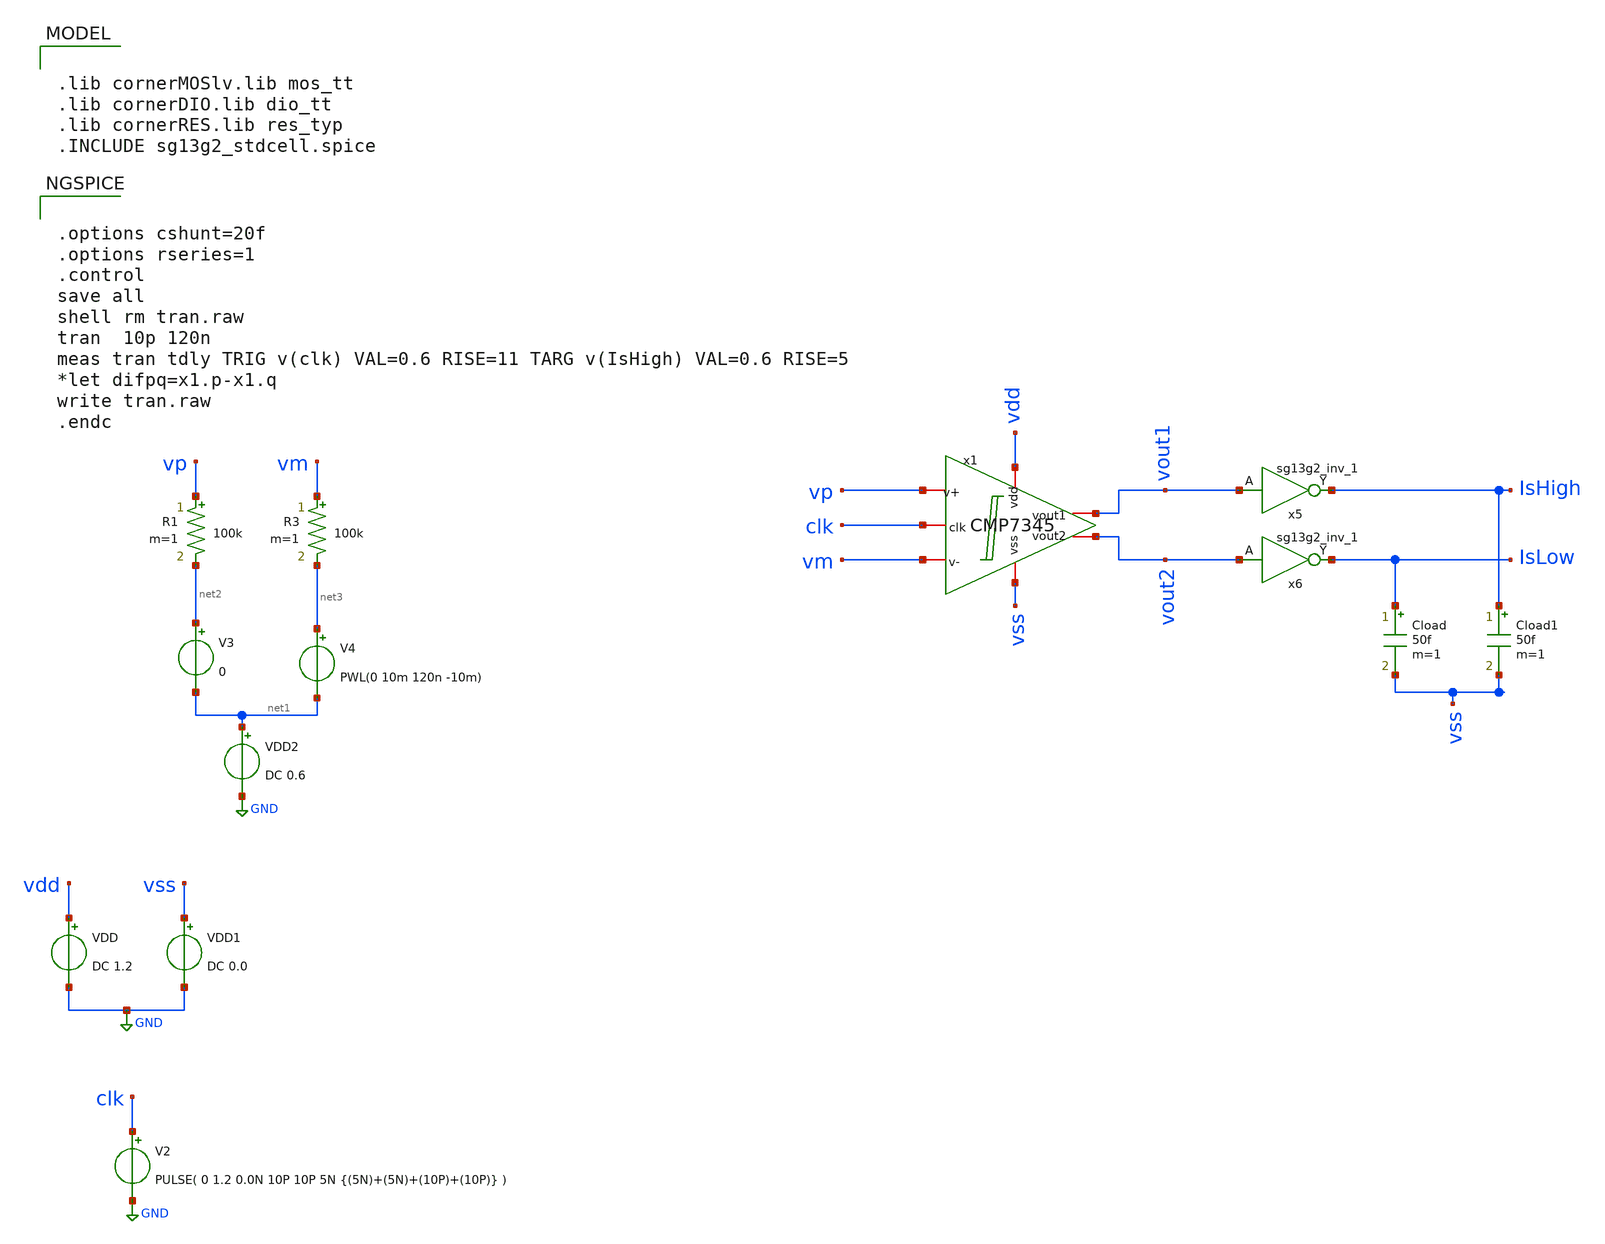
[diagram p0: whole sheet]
** sch_path: CMP7345-main/testbenches/noise/xschem/CMP7345_kickback.sch
**.subckt CMP7345_kickback
VDD vdd GND DC 1.2
Cload IsLow vss 50f m=1
x1 vdd vout1 vout2 vp vm clk vss CMP7345
VDD1 vss GND DC 0.0
Cload1 IsHigh vss 50f m=1
V2 clk GND PULSE( 0 1.2 0.0N 10P 10P 5N {(5N)+(5N)+(10P)+(10P)} )
V3 net2 net1 0
VDD2 net1 GND DC 0.6
x5 IsHigh vout1 VDD VSS sg13g2_inv_1
x6 IsLow vout2 VDD VSS sg13g2_inv_1
V4 net3 net1 PWL(0 10m 120n -10m)
R3 vm net3 100k m=1
R1 vp net2 100k m=1
**** begin user architecture code

.lib cornerMOSlv.lib mos_tt
.lib cornerDIO.lib dio_tt
.lib cornerRES.lib res_typ
.INCLUDE sg13g2_stdcell.spice



.options cshunt=20f
.options rseries=1
.control
save all
shell rm tran.raw
tran  10p 120n
meas tran tdly TRIG v(clk) VAL=0.6 RISE=11 TARG v(IsHigh) VAL=0.6 RISE=5
*let difpq=x1.p-x1.q
write tran.raw
.endc


**** end user architecture code
**.ends

* expanding   symbol:  sg13g2_stdcells/sg13g2_inv_1.sym # of pins=2
** sym_path: sg13g2_stdcells/sg13g2_inv_1.sym
** sch_path: sg13g2_stdcells/sg13g2_inv_1.sch
.subckt sg13g2_inv_1 Y A VDD VSS
*.opin Y
*.ipin A
*.iopin VDD
*.iopin VSS
XM1 Y A VSS VSS sg13_lv_nmos w=740.00n l=130.00n ng=1 m=1 mm_ok=1
XM2 Y A VDD VDD sg13_lv_pmos w=1.12u l=130.00n ng=1 m=1 mm_ok=1
.ends

.GLOBAL GND
.end
